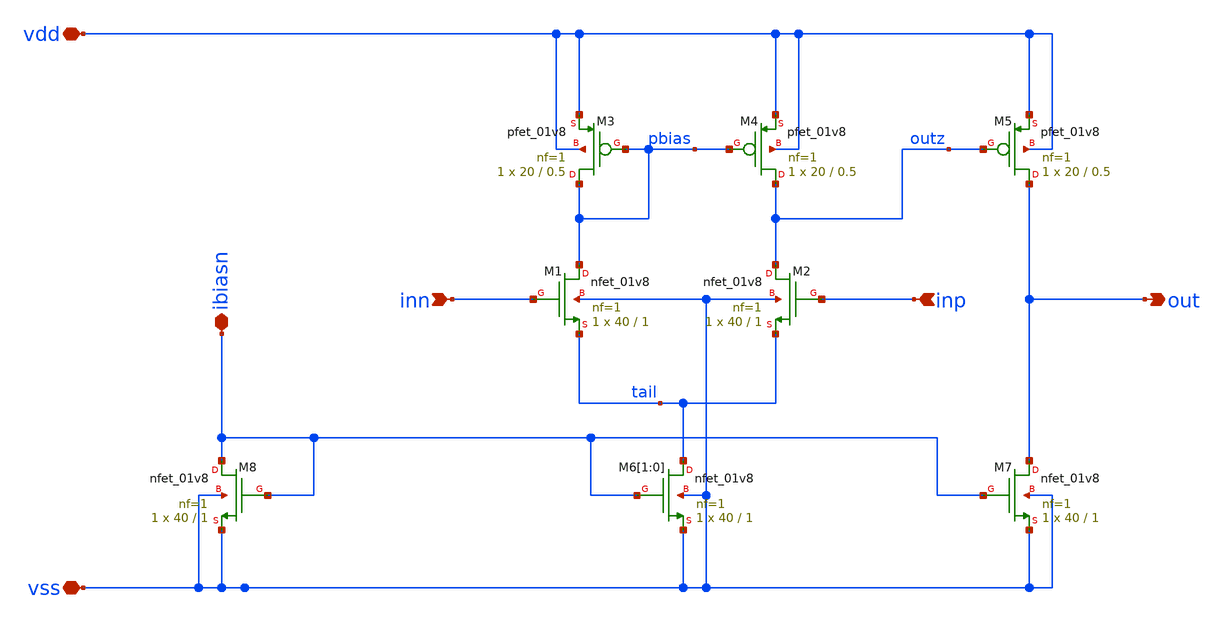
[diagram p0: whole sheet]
** sch_path: sky130A/HelloWorld/xschem/opamp.sch
**.subckt opamp inn inp vdd vss ibiasn out
*.ipin inn
*.ipin inp
*.iopin vdd
*.iopin vss
*.iopin ibiasn
*.opin out
XM1 pbias inn tail vss sky130_fd_pr__nfet_01v8 L=1 W=40 nf=1 ad='int((nf+1)/2) * W/nf * 0.29' as='int((nf+2)/2) * W/nf * 0.29'
+ pd='2*int((nf+1)/2) * (W/nf + 0.29)' ps='2*int((nf+2)/2) * (W/nf + 0.29)' nrd='0.29 / W' nrs='0.29 / W'
+ sa=0 sb=0 sd=0 mult=1 m=1
XM2 outz inp tail vss sky130_fd_pr__nfet_01v8 L=1 W=40 nf=1 ad='int((nf+1)/2) * W/nf * 0.29' as='int((nf+2)/2) * W/nf * 0.29'
+ pd='2*int((nf+1)/2) * (W/nf + 0.29)' ps='2*int((nf+2)/2) * (W/nf + 0.29)' nrd='0.29 / W' nrs='0.29 / W'
+ sa=0 sb=0 sd=0 mult=1 m=1
XM3 pbias pbias vdd vdd sky130_fd_pr__pfet_01v8 L=0.5 W=20 nf=1 ad='int((nf+1)/2) * W/nf * 0.29' as='int((nf+2)/2) * W/nf * 0.29'
+ pd='2*int((nf+1)/2) * (W/nf + 0.29)' ps='2*int((nf+2)/2) * (W/nf + 0.29)' nrd='0.29 / W' nrs='0.29 / W'
+ sa=0 sb=0 sd=0 mult=1 m=1
XM4 outz pbias vdd vdd sky130_fd_pr__pfet_01v8 L=0.5 W=20 nf=1 ad='int((nf+1)/2) * W/nf * 0.29' as='int((nf+2)/2) * W/nf * 0.29'
+ pd='2*int((nf+1)/2) * (W/nf + 0.29)' ps='2*int((nf+2)/2) * (W/nf + 0.29)' nrd='0.29 / W' nrs='0.29 / W'
+ sa=0 sb=0 sd=0 mult=1 m=1
XM5 out outz vdd vdd sky130_fd_pr__pfet_01v8 L=0.5 W=20 nf=1 ad='int((nf+1)/2) * W/nf * 0.29' as='int((nf+2)/2) * W/nf * 0.29'
+ pd='2*int((nf+1)/2) * (W/nf + 0.29)' ps='2*int((nf+2)/2) * (W/nf + 0.29)' nrd='0.29 / W' nrs='0.29 / W'
+ sa=0 sb=0 sd=0 mult=1 m=1
XM6[1] tail ibiasn vss vss sky130_fd_pr__nfet_01v8 L=1 W=40 nf=1 ad='int((nf+1)/2) * W/nf * 0.29' as='int((nf+2)/2) * W/nf * 0.29'
+ pd='2*int((nf+1)/2) * (W/nf + 0.29)' ps='2*int((nf+2)/2) * (W/nf + 0.29)' nrd='0.29 / W' nrs='0.29 / W'
+ sa=0 sb=0 sd=0 mult=1 m=1
XM6[0] tail ibiasn vss vss sky130_fd_pr__nfet_01v8 L=1 W=40 nf=1 ad='int((nf+1)/2) * W/nf * 0.29' as='int((nf+2)/2) * W/nf * 0.29'
+ pd='2*int((nf+1)/2) * (W/nf + 0.29)' ps='2*int((nf+2)/2) * (W/nf + 0.29)' nrd='0.29 / W' nrs='0.29 / W'
+ sa=0 sb=0 sd=0 mult=1 m=1
XM7 out ibiasn vss vss sky130_fd_pr__nfet_01v8 L=1 W=40 nf=1 ad='int((nf+1)/2) * W/nf * 0.29' as='int((nf+2)/2) * W/nf * 0.29'
+ pd='2*int((nf+1)/2) * (W/nf + 0.29)' ps='2*int((nf+2)/2) * (W/nf + 0.29)' nrd='0.29 / W' nrs='0.29 / W'
+ sa=0 sb=0 sd=0 mult=1 m=1
XM8 ibiasn ibiasn vss vss sky130_fd_pr__nfet_01v8 L=1 W=40 nf=1 ad='int((nf+1)/2) * W/nf * 0.29' as='int((nf+2)/2) * W/nf * 0.29'
+ pd='2*int((nf+1)/2) * (W/nf + 0.29)' ps='2*int((nf+2)/2) * (W/nf + 0.29)' nrd='0.29 / W' nrs='0.29 / W'
+ sa=0 sb=0 sd=0 mult=1 m=1
**.ends
.end
